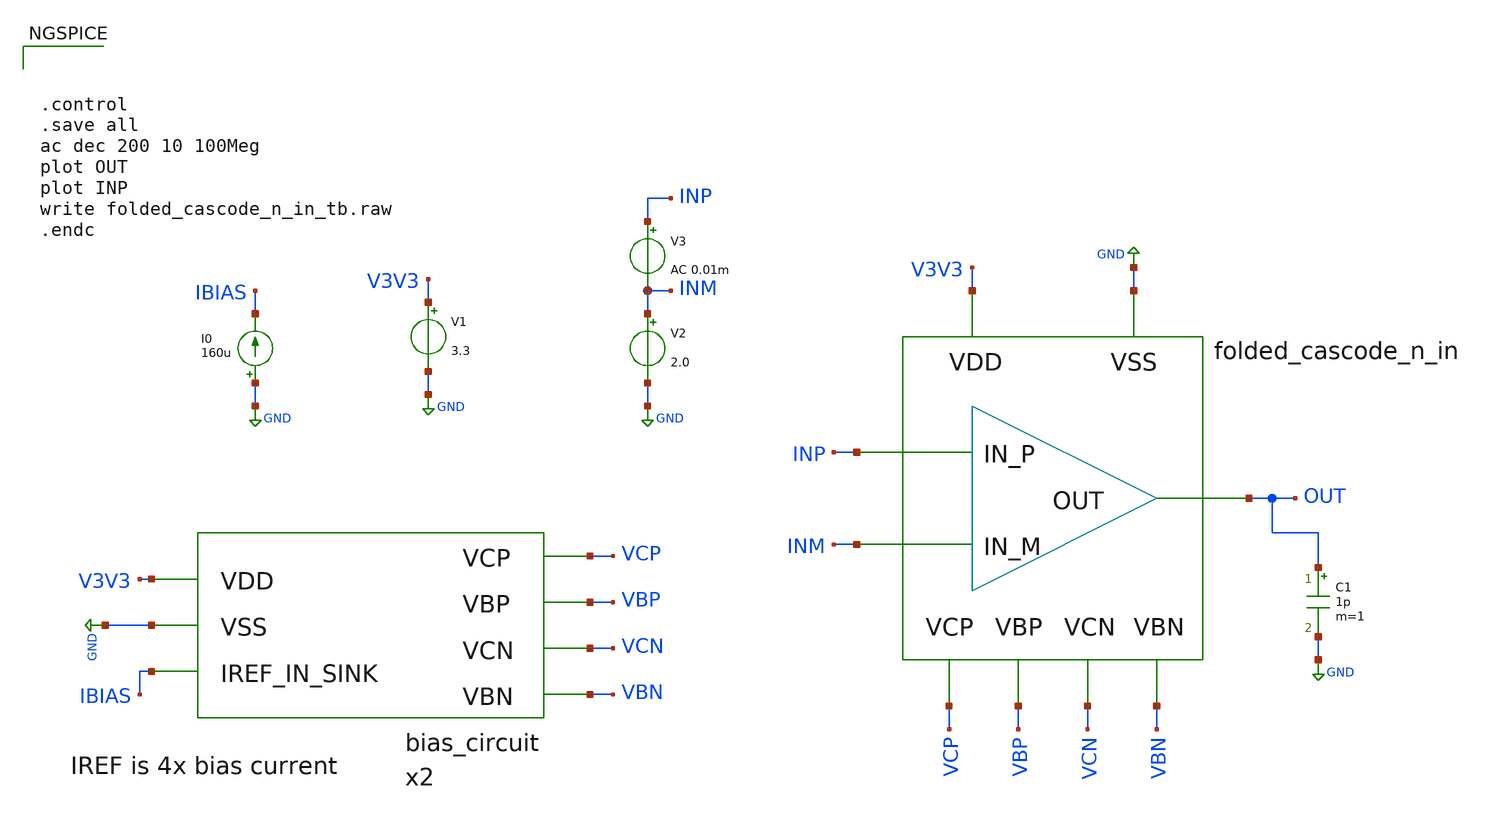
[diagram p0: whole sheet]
** sch_path: design/folded-cascode-n-in/folded_cascode_n_in_tb.sch
**.subckt folded_cascode_n_in_tb
V1 V3V3 GND 3.3
I0 GND IBIAS 160u
V2 INM GND 2.0
V3 INP INM AC 0.01m
C1 OUT GND 1p m=1
x2 V3V3 GND VCP VBP VCN VBN IBIAS bias_circuit
**** begin user architecture code



.control
.save all
ac dec 200 10 100Meg
plot OUT
plot INP
write folded_cascode_n_in_tb.raw
.endc



.include $::SKYWATER_MODELS/cells/nfet_01v8/sky130_fd_pr__nfet_01v8__tt.corner.spice
.include $::SKYWATER_MODELS/cells/nfet_01v8_lvt/sky130_fd_pr__nfet_01v8_lvt__tt.corner.spice
.include $::SKYWATER_MODELS/cells/pfet_01v8/sky130_fd_pr__pfet_01v8__tt.corner.spice
.include $::SKYWATER_MODELS/cells/nfet_03v3_nvt/sky130_fd_pr__nfet_03v3_nvt__tt.corner.spice
.include $::SKYWATER_MODELS/cells/nfet_05v0_nvt/sky130_fd_pr__nfet_05v0_nvt__tt.corner.spice
.include $::SKYWATER_MODELS/cells/esd_nfet_01v8/sky130_fd_pr__esd_nfet_01v8__tt.corner.spice
.include $::SKYWATER_MODELS/cells/pfet_01v8_lvt/sky130_fd_pr__pfet_01v8_lvt__tt.corner.spice
.include $::SKYWATER_MODELS/cells/pfet_01v8_hvt/sky130_fd_pr__pfet_01v8_hvt__tt.corner.spice
.include $::SKYWATER_MODELS/cells/esd_pfet_g5v0d10v5/sky130_fd_pr__esd_pfet_g5v0d10v5__tt.corner.spice
.include $::SKYWATER_MODELS/cells/pfet_g5v0d10v5/sky130_fd_pr__pfet_g5v0d10v5__tt.corner.spice
.include $::SKYWATER_MODELS/cells/pfet_g5v0d16v0/sky130_fd_pr__pfet_g5v0d16v0__tt.corner.spice
.include $::SKYWATER_MODELS/cells/nfet_g5v0d10v5/sky130_fd_pr__nfet_g5v0d10v5__tt.corner.spice
.include $::SKYWATER_MODELS/cells/nfet_g5v0d16v0/sky130_fd_pr__nfet_g5v0d16v0__tt_discrete.corner.spice
.include $::SKYWATER_MODELS/cells/esd_nfet_g5v0d10v5/sky130_fd_pr__esd_nfet_g5v0d10v5__tt.corner.spice
.include $::SKYWATER_MODELS/models/corners/tt/nonfet.spice
* Mismatch parameters
.include $::SKYWATER_MODELS/cells/nfet_01v8/sky130_fd_pr__nfet_01v8__mismatch.corner.spice
.include $::SKYWATER_MODELS/cells/pfet_01v8/sky130_fd_pr__pfet_01v8__mismatch.corner.spice
.include $::SKYWATER_MODELS/cells/nfet_01v8_lvt/sky130_fd_pr__nfet_01v8_lvt__mismatch.corner.spice
.include $::SKYWATER_MODELS/cells/pfet_01v8_lvt/sky130_fd_pr__pfet_01v8_lvt__mismatch.corner.spice
.include $::SKYWATER_MODELS/cells/pfet_01v8_hvt/sky130_fd_pr__pfet_01v8_hvt__mismatch.corner.spice
.include $::SKYWATER_MODELS/cells/nfet_g5v0d10v5/sky130_fd_pr__nfet_g5v0d10v5__mismatch.corner.spice
.include $::SKYWATER_MODELS/cells/pfet_g5v0d10v5/sky130_fd_pr__pfet_g5v0d10v5__mismatch.corner.spice
.include $::SKYWATER_MODELS/cells/nfet_05v0_nvt/sky130_fd_pr__nfet_05v0_nvt__mismatch.corner.spice
.include $::SKYWATER_MODELS/cells/nfet_03v3_nvt/sky130_fd_pr__nfet_03v3_nvt__mismatch.corner.spice
* Resistor$::SKYWATER_MODELS/Capacitor
.include $::SKYWATER_MODELS/models/r+c/res_typical__cap_typical.spice
.include $::SKYWATER_MODELS/models/r+c/res_typical__cap_typical__lin.spice
* Special cells
.include $::SKYWATER_MODELS/models/corners/tt/specialized_cells.spice
* All models
.include $::SKYWATER_MODELS/models/all.spice
* Corner
.include $::SKYWATER_MODELS/models/corners/tt/rf.spice

**** end user architecture code
**.ends

* expanding   symbol:  /home/wbraun/projects/open-pmic/design/bias-circuit/bias_circuit.sym # of
*+ pins=7
** sym_path: design/bias-circuit/bias_circuit.sym
** sch_path: design/bias-circuit/bias_circuit.sch
.subckt bias_circuit VDD VSS VCP VBP VCN VBN IREF_IN_SINK
*.ipin IREF_IN_SINK
*.ipin VCN
*.ipin VSS
*.ipin VDD
*.ipin VCP
*.ipin VBP
*.ipin VBN
XM2 VBP VBP VDD VDD sky130_fd_pr__pfet_g5v0d10v5 L=0.5 W=1 nf=1 ad='int((nf+1)/2) * W/nf * 0.29' as='int((nf+2)/2) * W/nf * 0.29'
+ pd='2*int((nf+1)/2) * (W/nf + 0.29)' ps='2*int((nf+2)/2) * (W/nf + 0.29)' nrd='0.29 / W' nrs='0.29 / W'
+ sa=0 sb=0 sd=0 mult=1 m=1
XM3 net1 VBP VDD VDD sky130_fd_pr__pfet_g5v0d10v5 L=0.5 W=1 nf=1 ad='int((nf+1)/2) * W/nf * 0.29' as='int((nf+2)/2) * W/nf * 0.29'
+ pd='2*int((nf+1)/2) * (W/nf + 0.29)' ps='2*int((nf+2)/2) * (W/nf + 0.29)' nrd='0.29 / W' nrs='0.29 / W'
+ sa=0 sb=0 sd=0 mult=1 m=1
XM4 VCN VBP VDD VDD sky130_fd_pr__pfet_g5v0d10v5 L=0.5 W=1 nf=1 ad='int((nf+1)/2) * W/nf * 0.29' as='int((nf+2)/2) * W/nf * 0.29'
+ pd='2*int((nf+1)/2) * (W/nf + 0.29)' ps='2*int((nf+2)/2) * (W/nf + 0.29)' nrd='0.29 / W' nrs='0.29 / W'
+ sa=0 sb=0 sd=0 mult=1 m=1
XM5 net1 net1 net2 VSS sky130_fd_pr__nfet_g5v0d10v5 L=0.5 W=1 nf=1 ad='int((nf+1)/2) * W/nf * 0.29' as='int((nf+2)/2) * W/nf * 0.29'
+ pd='2*int((nf+1)/2) * (W/nf + 0.29)' ps='2*int((nf+2)/2) * (W/nf + 0.29)' nrd='0.29 / W' nrs='0.29 / W'
+ sa=0 sb=0 sd=0 mult=1 m=1
XM6 net2 net1 VSS VSS sky130_fd_pr__nfet_g5v0d10v5 L=0.5 W=1 nf=1 ad='int((nf+1)/2) * W/nf * 0.29' as='int((nf+2)/2) * W/nf * 0.29'
+ pd='2*int((nf+1)/2) * (W/nf + 0.29)' ps='2*int((nf+2)/2) * (W/nf + 0.29)' nrd='0.29 / W' nrs='0.29 / W'
+ sa=0 sb=0 sd=0 mult=1 m=1
XM7 VCN VCN net2 VSS sky130_fd_pr__nfet_g5v0d10v5 L=0.5 W=1 nf=1 ad='int((nf+1)/2) * W/nf * 0.29' as='int((nf+2)/2) * W/nf * 0.29'
+ pd='2*int((nf+1)/2) * (W/nf + 0.29)' ps='2*int((nf+2)/2) * (W/nf + 0.29)' nrd='0.29 / W' nrs='0.29 / W'
+ sa=0 sb=0 sd=0 mult=1 m=1
XM8 VBN VBN VSS VSS sky130_fd_pr__nfet_g5v0d10v5 L=0.5 W=1 nf=1 ad='int((nf+1)/2) * W/nf * 0.29' as='int((nf+2)/2) * W/nf * 0.29'
+ pd='2*int((nf+1)/2) * (W/nf + 0.29)' ps='2*int((nf+2)/2) * (W/nf + 0.29)' nrd='0.29 / W' nrs='0.29 / W'
+ sa=0 sb=0 sd=0 mult=1 m=1
XM9 VBN VBP VDD VDD sky130_fd_pr__pfet_g5v0d10v5 L=0.5 W=1 nf=1 ad='int((nf+1)/2) * W/nf * 0.29' as='int((nf+2)/2) * W/nf * 0.29'
+ pd='2*int((nf+1)/2) * (W/nf + 0.29)' ps='2*int((nf+2)/2) * (W/nf + 0.29)' nrd='0.29 / W' nrs='0.29 / W'
+ sa=0 sb=0 sd=0 mult=1 m=1
XM10 net3 VBN VSS VSS sky130_fd_pr__nfet_g5v0d10v5 L=0.5 W=1 nf=1 ad='int((nf+1)/2) * W/nf * 0.29' as='int((nf+2)/2) * W/nf * 0.29'
+ pd='2*int((nf+1)/2) * (W/nf + 0.29)' ps='2*int((nf+2)/2) * (W/nf + 0.29)' nrd='0.29 / W' nrs='0.29 / W'
+ sa=0 sb=0 sd=0 mult=1 m=1
XM11 VCP VBN VSS VSS sky130_fd_pr__nfet_g5v0d10v5 L=0.5 W=1 nf=1 ad='int((nf+1)/2) * W/nf * 0.29' as='int((nf+2)/2) * W/nf * 0.29'
+ pd='2*int((nf+1)/2) * (W/nf + 0.29)' ps='2*int((nf+2)/2) * (W/nf + 0.29)' nrd='0.29 / W' nrs='0.29 / W'
+ sa=0 sb=0 sd=0 mult=1 m=1
XM12 net3 net3 net4 VDD sky130_fd_pr__pfet_g5v0d10v5 L=0.5 W=1 nf=1 ad='int((nf+1)/2) * W/nf * 0.29'
+ as='int((nf+2)/2) * W/nf * 0.29' pd='2*int((nf+1)/2) * (W/nf + 0.29)' ps='2*int((nf+2)/2) * (W/nf + 0.29)'
+ nrd='0.29 / W' nrs='0.29 / W' sa=0 sb=0 sd=0 mult=1 m=1
XM13 VCP VCP net4 VDD sky130_fd_pr__pfet_g5v0d10v5 L=0.5 W=1 nf=1 ad='int((nf+1)/2) * W/nf * 0.29' as='int((nf+2)/2) * W/nf * 0.29'
+ pd='2*int((nf+1)/2) * (W/nf + 0.29)' ps='2*int((nf+2)/2) * (W/nf + 0.29)' nrd='0.29 / W' nrs='0.29 / W'
+ sa=0 sb=0 sd=0 mult=1 m=1
XM14 net4 net3 VDD VDD sky130_fd_pr__pfet_g5v0d10v5 L=0.5 W=1 nf=1 ad='int((nf+1)/2) * W/nf * 0.29' as='int((nf+2)/2) * W/nf * 0.29'
+ pd='2*int((nf+1)/2) * (W/nf + 0.29)' ps='2*int((nf+2)/2) * (W/nf + 0.29)' nrd='0.29 / W' nrs='0.29 / W'
+ sa=0 sb=0 sd=0 mult=1 m=1
XM1 VBP IREF_IN_SINK VSS VSS sky130_fd_pr__nfet_g5v0d10v5 L=0.5 W=1 nf=1 ad='int((nf+1)/2) * W/nf * 0.29'
+ as='int((nf+2)/2) * W/nf * 0.29' pd='2*int((nf+1)/2) * (W/nf + 0.29)' ps='2*int((nf+2)/2) * (W/nf + 0.29)'
+ nrd='0.29 / W' nrs='0.29 / W' sa=0 sb=0 sd=0 mult=1 m=1
XM15 IREF_IN_SINK IREF_IN_SINK VSS VSS sky130_fd_pr__nfet_g5v0d10v5 L=0.5 W=1 nf=1 ad='int((nf+1)/2) * W/nf * 0.29'
+ as='int((nf+2)/2) * W/nf * 0.29' pd='2*int((nf+1)/2) * (W/nf + 0.29)' ps='2*int((nf+2)/2) * (W/nf + 0.29)'
+ nrd='0.29 / W' nrs='0.29 / W' sa=0 sb=0 sd=0 mult=1 m=1
.ends

.GLOBAL GND
**** begin user architecture code
[sky130_models]
**** end user architecture code
.end
